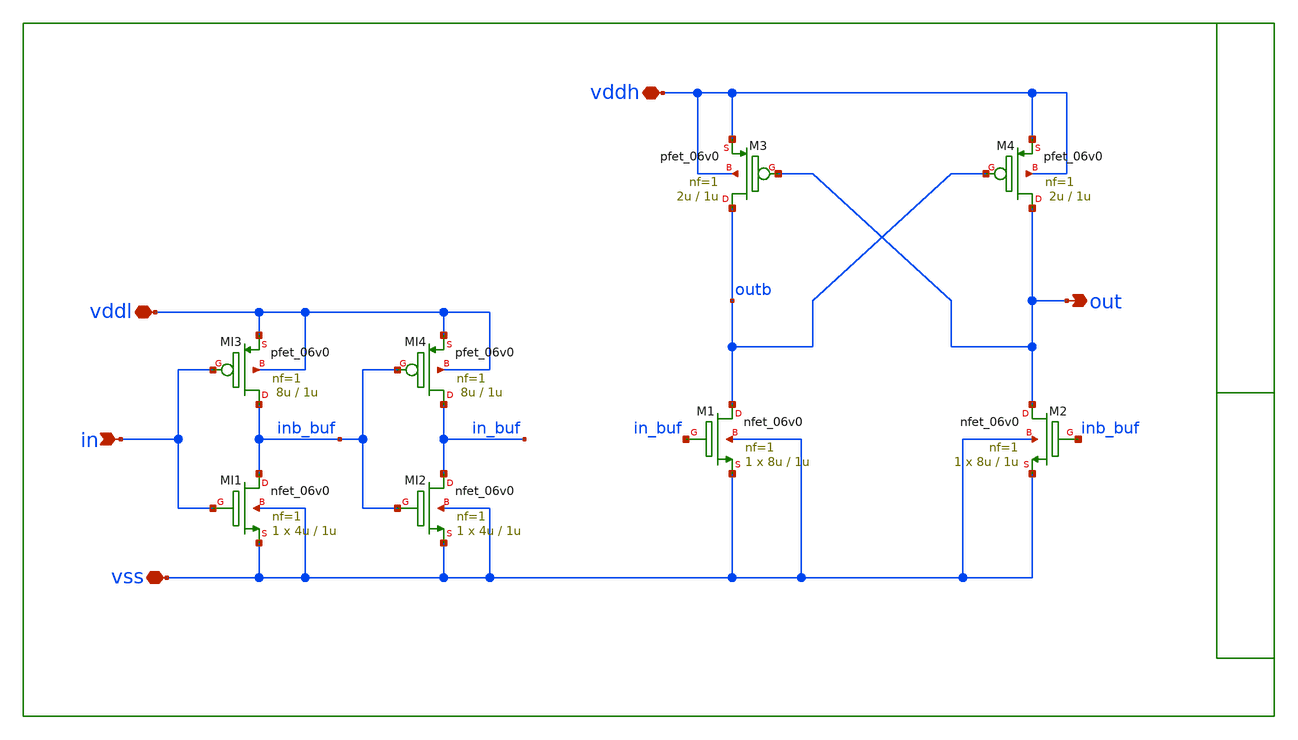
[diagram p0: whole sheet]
** sch_path: xschem/sch/levelshifter/levelshifter/levelshifter.sch
**.subckt levelshifter vddl in out vddh vss
*.iopin vddl
*.ipin in
*.opin out
*.iopin vddh
*.iopin vss
XMI1 inb_buf in vss vss nfet_06v0 L=1u W=4u nf=1 ad='int((nf+1)/2) * W/nf * 0.18u' as='int((nf+2)/2) * W/nf * 0.18u'
+ pd='2*int((nf+1)/2) * (W/nf + 0.18u)' ps='2*int((nf+2)/2) * (W/nf + 0.18u)' nrd='0.18u / W' nrs='0.18u / W'
+ sa=0 sb=0 sd=0 m=1 par=1
XMI2 in_buf inb_buf vss vss nfet_06v0 L=1u W=4u nf=1 ad='int((nf+1)/2) * W/nf * 0.18u' as='int((nf+2)/2) * W/nf * 0.18u'
+ pd='2*int((nf+1)/2) * (W/nf + 0.18u)' ps='2*int((nf+2)/2) * (W/nf + 0.18u)' nrd='0.18u / W' nrs='0.18u / W'
+ sa=0 sb=0 sd=0 m=1 par=1
XM1 outb in_buf vss vss nfet_06v0 L=1u W=8u nf=1 ad='int((nf+1)/2) * W/nf * 0.18u' as='int((nf+2)/2) * W/nf * 0.18u'
+ pd='2*int((nf+1)/2) * (W/nf + 0.18u)' ps='2*int((nf+2)/2) * (W/nf + 0.18u)' nrd='0.18u / W' nrs='0.18u / W'
+ sa=0 sb=0 sd=0 m=1 par=1
XM2 out inb_buf vss vss nfet_06v0 L=1u W=8u nf=1 ad='int((nf+1)/2) * W/nf * 0.18u' as='int((nf+2)/2) * W/nf * 0.18u'
+ pd='2*int((nf+1)/2) * (W/nf + 0.18u)' ps='2*int((nf+2)/2) * (W/nf + 0.18u)' nrd='0.18u / W' nrs='0.18u / W'
+ sa=0 sb=0 sd=0 m=1 par=1
XMI3 inb_buf in vddl vddl pfet_06v0 L=1u W=8u nf=1 ad='int((nf+1)/2) * W/nf * 0.18u' as='int((nf+2)/2) * W/nf * 0.18u'
+ pd='2*int((nf+1)/2) * (W/nf + 0.18u)' ps='2*int((nf+2)/2) * (W/nf + 0.18u)' nrd='0.18u / W' nrs='0.18u / W'
+ sa=0 sb=0 sd=0 m=1 par=1
XMI4 in_buf inb_buf vddl vddl pfet_06v0 L=1u W=8u nf=1 ad='int((nf+1)/2) * W/nf * 0.18u' as='int((nf+2)/2) * W/nf * 0.18u'
+ pd='2*int((nf+1)/2) * (W/nf + 0.18u)' ps='2*int((nf+2)/2) * (W/nf + 0.18u)' nrd='0.18u / W' nrs='0.18u / W'
+ sa=0 sb=0 sd=0 m=1 par=1
XM3 outb out vddh vddh pfet_06v0 L=1u W=2u nf=1 ad='int((nf+1)/2) * W/nf * 0.18u' as='int((nf+2)/2) * W/nf * 0.18u'
+ pd='2*int((nf+1)/2) * (W/nf + 0.18u)' ps='2*int((nf+2)/2) * (W/nf + 0.18u)' nrd='0.18u / W' nrs='0.18u / W'
+ sa=0 sb=0 sd=0 m=1 par=1
XM4 out outb vddh vddh pfet_06v0 L=1u W=2u nf=1 ad='int((nf+1)/2) * W/nf * 0.18u' as='int((nf+2)/2) * W/nf * 0.18u'
+ pd='2*int((nf+1)/2) * (W/nf + 0.18u)' ps='2*int((nf+2)/2) * (W/nf + 0.18u)' nrd='0.18u / W' nrs='0.18u / W'
+ sa=0 sb=0 sd=0 m=1 par=1
**.ends
.end
